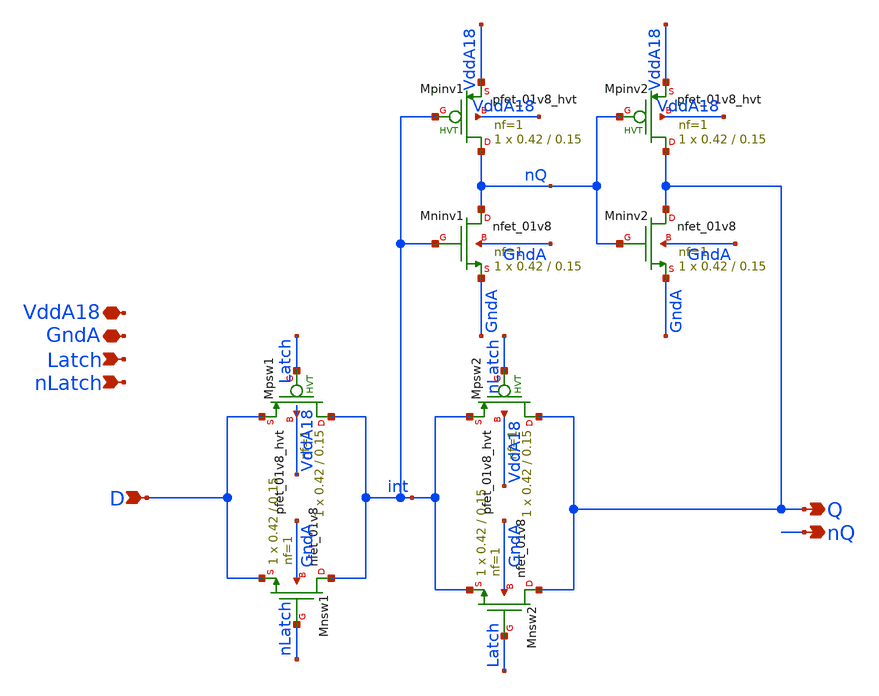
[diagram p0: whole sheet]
** sch_path: analog/xschem/BiasLatch.sch
**.subckt BiasLatch D Latch nLatch Q GndA VddA18 nQ
*.ipin D
*.ipin Latch
*.ipin nLatch
*.opin Q
*.iopin GndA
*.iopin VddA18
*.opin nQ
XMnsw1 int nLatch D GndA sky130_fd_pr__nfet_01v8 L=0.15 W=0.42 nf=1 ad='int((1 + 1)/2) * 0.42 / 1 * 0.29'
+ as='int((1 + 2)/2) * 0.42 / 1 * 0.29' pd='2*int((1 + 1)/2) * (0.42 / 1 + 0.29)' ps='2*int((1 + 2)/2) * (0.42 / 1 + 0.29)'
+ nrd='0.29 / 0.42 ' nrs='0.29 / 0.42 ' sa=0 sb=0 sd=0 mult=1 m=1
XMpsw1 int Latch D VddA18 sky130_fd_pr__pfet_01v8_hvt L=0.15 W=0.42 nf=1 ad='int((1 + 1)/2) * 0.42 / 1 * 0.29'
+ as='int((1 + 2)/2) * 0.42 / 1 * 0.29' pd='2*int((1 + 1)/2) * (0.42 / 1 + 0.29)' ps='2*int((1 + 2)/2) * (0.42 / 1 + 0.29)'
+ nrd='0.29 / 0.42 ' nrs='0.29 / 0.42 ' sa=0 sb=0 sd=0 mult=1 m=1
XMnsw2 Q Latch int GndA sky130_fd_pr__nfet_01v8 L=0.15 W=0.42 nf=1 ad='int((1 + 1)/2) * 0.42 / 1 * 0.29'
+ as='int((1 + 2)/2) * 0.42 / 1 * 0.29' pd='2*int((1 + 1)/2) * (0.42 / 1 + 0.29)' ps='2*int((1 + 2)/2) * (0.42 / 1 + 0.29)'
+ nrd='0.29 / 0.42 ' nrs='0.29 / 0.42 ' sa=0 sb=0 sd=0 mult=1 m=1
XMpsw2 Q nLatch int VddA18 sky130_fd_pr__pfet_01v8_hvt L=0.15 W=0.42 nf=1 ad='int((1 + 1)/2) * 0.42 / 1 * 0.29'
+ as='int((1 + 2)/2) * 0.42 / 1 * 0.29' pd='2*int((1 + 1)/2) * (0.42 / 1 + 0.29)' ps='2*int((1 + 2)/2) * (0.42 / 1 + 0.29)'
+ nrd='0.29 / 0.42 ' nrs='0.29 / 0.42 ' sa=0 sb=0 sd=0 mult=1 m=1
XMpinv1 nQ int VddA18 VddA18 sky130_fd_pr__pfet_01v8_hvt L=0.15 W=0.42 nf=1 ad='int((1 + 1)/2) * 0.42 / 1 * 0.29'
+ as='int((1 + 2)/2) * 0.42 / 1 * 0.29' pd='2*int((1 + 1)/2) * (0.42 / 1 + 0.29)' ps='2*int((1 + 2)/2) * (0.42 / 1 + 0.29)'
+ nrd='0.29 / 0.42 ' nrs='0.29 / 0.42 ' sa=0 sb=0 sd=0 mult=1 m=1
XMpinv2 Q nQ VddA18 VddA18 sky130_fd_pr__pfet_01v8_hvt L=0.15 W=0.42 nf=1 ad='int((1 + 1)/2) * 0.42 / 1 * 0.29'
+ as='int((1 + 2)/2) * 0.42 / 1 * 0.29' pd='2*int((1 + 1)/2) * (0.42 / 1 + 0.29)' ps='2*int((1 + 2)/2) * (0.42 / 1 + 0.29)'
+ nrd='0.29 / 0.42 ' nrs='0.29 / 0.42 ' sa=0 sb=0 sd=0 mult=1 m=1
XMninv1 nQ int GndA GndA sky130_fd_pr__nfet_01v8 L=0.15 W=0.42 nf=1 ad='int((1 + 1)/2) * 0.42 / 1 * 0.29'
+ as='int((1 + 2)/2) * 0.42 / 1 * 0.29' pd='2*int((1 + 1)/2) * (0.42 / 1 + 0.29)' ps='2*int((1 + 2)/2) * (0.42 / 1 + 0.29)'
+ nrd='0.29 / 0.42 ' nrs='0.29 / 0.42 ' sa=0 sb=0 sd=0 mult=1 m=1
XMninv2 Q nQ GndA GndA sky130_fd_pr__nfet_01v8 L=0.15 W=0.42 nf=1 ad='int((1 + 1)/2) * 0.42 / 1 * 0.29'
+ as='int((1 + 2)/2) * 0.42 / 1 * 0.29' pd='2*int((1 + 1)/2) * (0.42 / 1 + 0.29)' ps='2*int((1 + 2)/2) * (0.42 / 1 + 0.29)'
+ nrd='0.29 / 0.42 ' nrs='0.29 / 0.42 ' sa=0 sb=0 sd=0 mult=1 m=1
**.ends
.end
